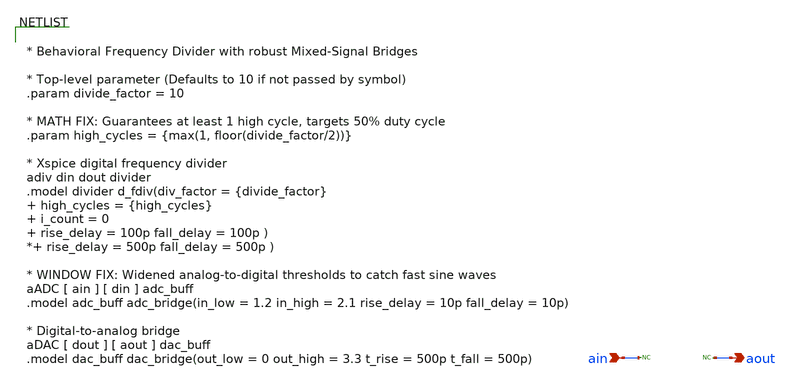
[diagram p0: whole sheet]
** sch_path: designs/libs/model_pll/freq_divider.sch
**.subckt freq_divider ain aout
*.ipin ain
*.opin aout
* noconn ain
* noconn aout
**** begin user architecture code


* Behavioral Frequency Divider with robust Mixed-Signal Bridges

* Top-level parameter (Defaults to 10 if not passed by symbol)
.param divide_factor = 10

* MATH FIX: Guarantees at least 1 high cycle, targets 50% duty cycle
.param high_cycles = {max(1, floor(divide_factor/2))}

* Xspice digital frequency divider
adiv din dout divider
.model divider d_fdiv(div_factor = {divide_factor}  high_cycles = {high_cycles}  i_count = 0  rise_delay
+ = 100p fall_delay = 100p )
*+ rise_delay = 500p fall_delay = 500p )

* WINDOW FIX: Widened analog-to-digital thresholds to catch fast sine waves
aADC [ ain ] [ din ] adc_buff
.model adc_buff adc_bridge(in_low = 1.2 in_high = 2.1 rise_delay = 10p fall_delay = 10p)

* Digital-to-analog bridge
aDAC [ dout ] [ aout ] dac_buff
.model dac_buff dac_bridge(out_low = 0 out_high = 3.3 t_rise = 500p t_fall = 500p)


**** end user architecture code
**.ends
.end
